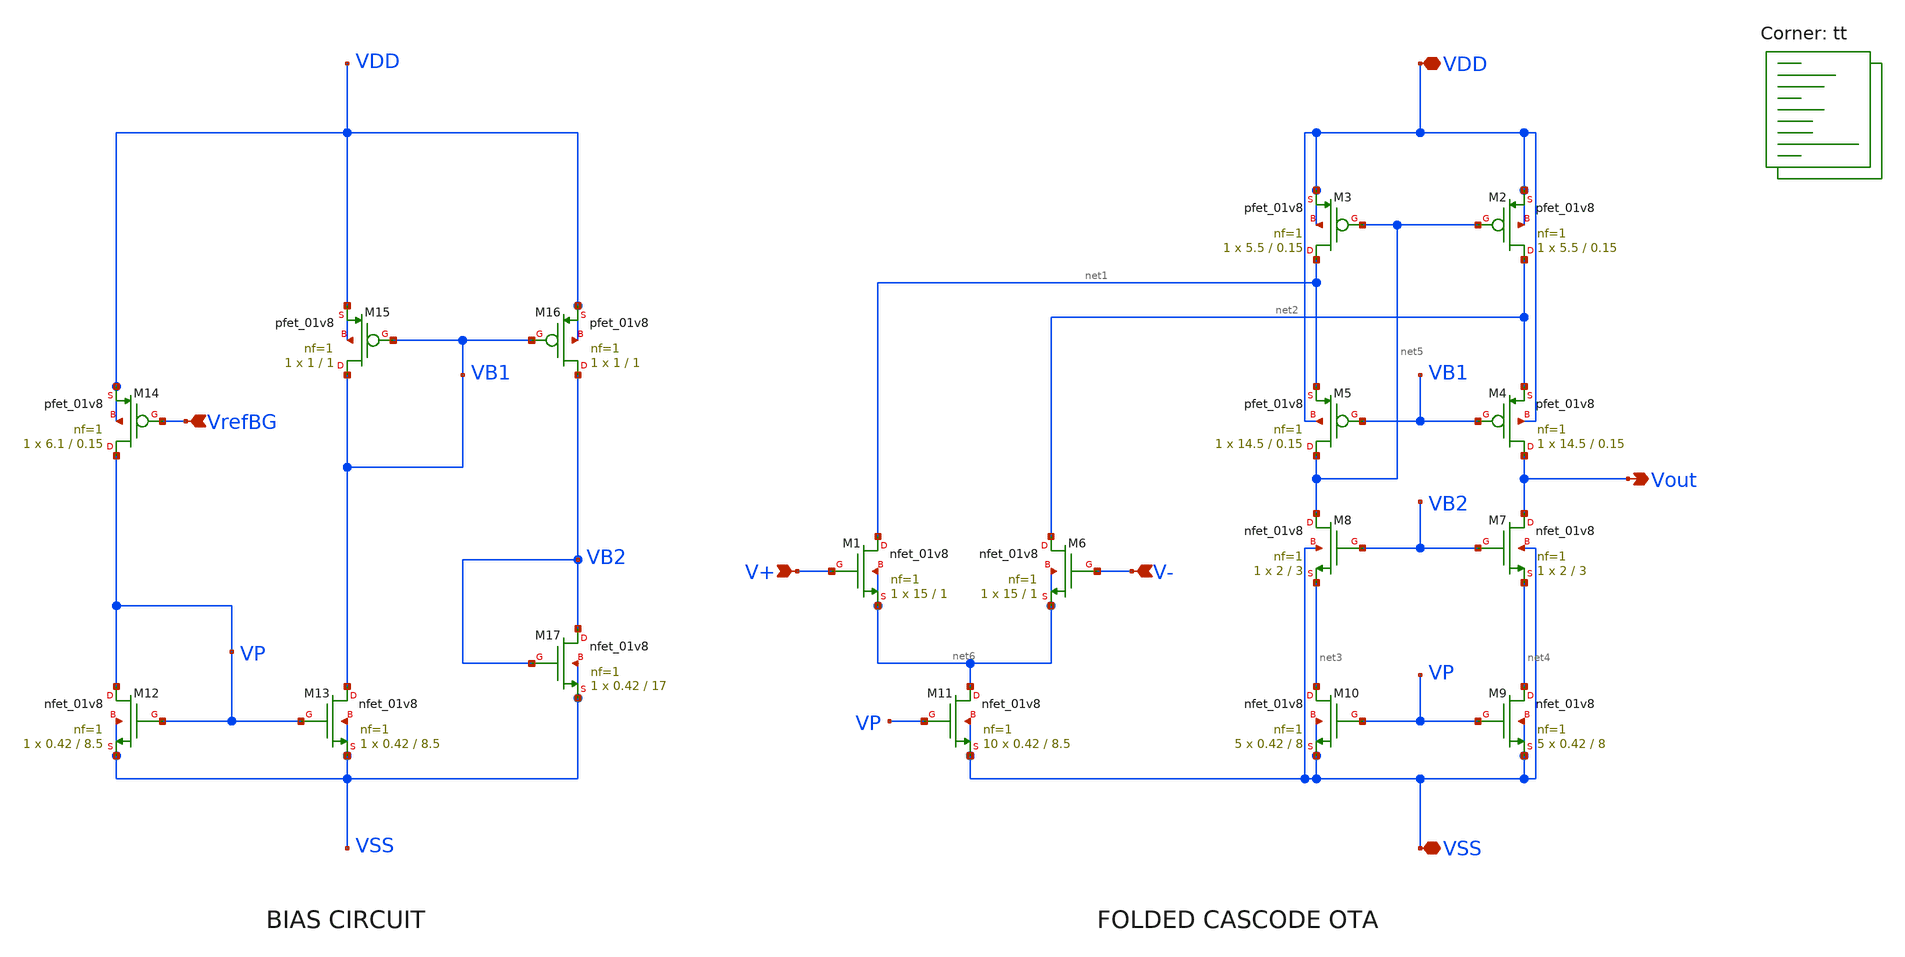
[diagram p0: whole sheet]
** sch_path: openfasoc/generators/curref-gen/sch/Folded_cascode_test.sch
**.subckt Folded_cascode_test Vout VSS V+ VDD V- VrefBG
*.opin Vout
*.iopin VSS
*.ipin V+
*.iopin VDD
*.ipin V-
*.ipin VrefBG
XM2 net2 net5 VDD VDD sky130_fd_pr__pfet_01v8 L=0.15 W=5.5 nf=1 ad='int((nf+1)/2) * W/nf * 0.29' as='int((nf+2)/2) * W/nf * 0.29'
+ pd='2*int((nf+1)/2) * (W/nf + 0.29)' ps='2*int((nf+2)/2) * (W/nf + 0.29)' nrd='0.29 / W' nrs='0.29 / W'
+ sa=0 sb=0 sd=0 mult=1 m=1
XM3 net1 net5 VDD VDD sky130_fd_pr__pfet_01v8 L=0.15 W=5.5 nf=1 ad='int((nf+1)/2) * W/nf * 0.29' as='int((nf+2)/2) * W/nf * 0.29'
+ pd='2*int((nf+1)/2) * (W/nf + 0.29)' ps='2*int((nf+2)/2) * (W/nf + 0.29)' nrd='0.29 / W' nrs='0.29 / W'
+ sa=0 sb=0 sd=0 mult=1 m=1
XM4 Vout VB1 net2 VDD sky130_fd_pr__pfet_01v8 L=0.15 W=14.5 nf=1 ad='int((nf+1)/2) * W/nf * 0.29' as='int((nf+2)/2) * W/nf * 0.29'
+ pd='2*int((nf+1)/2) * (W/nf + 0.29)' ps='2*int((nf+2)/2) * (W/nf + 0.29)' nrd='0.29 / W' nrs='0.29 / W'
+ sa=0 sb=0 sd=0 mult=1 m=1
XM5 net5 VB1 net1 VDD sky130_fd_pr__pfet_01v8 L=0.15 W=14.5 nf=1 ad='int((nf+1)/2) * W/nf * 0.29' as='int((nf+2)/2) * W/nf * 0.29'
+ pd='2*int((nf+1)/2) * (W/nf + 0.29)' ps='2*int((nf+2)/2) * (W/nf + 0.29)' nrd='0.29 / W' nrs='0.29 / W'
+ sa=0 sb=0 sd=0 mult=1 m=1
XM6 net2 V- net6 net6 sky130_fd_pr__nfet_01v8 L=1 W=15 nf=1 ad='int((nf+1)/2) * W/nf * 0.29' as='int((nf+2)/2) * W/nf * 0.29'
+ pd='2*int((nf+1)/2) * (W/nf + 0.29)' ps='2*int((nf+2)/2) * (W/nf + 0.29)' nrd='0.29 / W' nrs='0.29 / W'
+ sa=0 sb=0 sd=0 mult=1 m=1
XM7 Vout VB2 net4 VSS sky130_fd_pr__nfet_01v8 L=3 W=2 nf=1 ad='int((nf+1)/2) * W/nf * 0.29' as='int((nf+2)/2) * W/nf * 0.29'
+ pd='2*int((nf+1)/2) * (W/nf + 0.29)' ps='2*int((nf+2)/2) * (W/nf + 0.29)' nrd='0.29 / W' nrs='0.29 / W'
+ sa=0 sb=0 sd=0 mult=1 m=1
XM8 net5 VB2 net3 VSS sky130_fd_pr__nfet_01v8 L=3 W=2 nf=1 ad='int((nf+1)/2) * W/nf * 0.29' as='int((nf+2)/2) * W/nf * 0.29'
+ pd='2*int((nf+1)/2) * (W/nf + 0.29)' ps='2*int((nf+2)/2) * (W/nf + 0.29)' nrd='0.29 / W' nrs='0.29 / W'
+ sa=0 sb=0 sd=0 mult=1 m=1
XM9 net4 VP VSS VSS sky130_fd_pr__nfet_01v8 L=8 W=0.42 nf=1 ad='int((nf+1)/2) * W/nf * 0.29' as='int((nf+2)/2) * W/nf * 0.29'
+ pd='2*int((nf+1)/2) * (W/nf + 0.29)' ps='2*int((nf+2)/2) * (W/nf + 0.29)' nrd='0.29 / W' nrs='0.29 / W'
+ sa=0 sb=0 sd=0 mult=5 m=5
XM10 net3 VP VSS VSS sky130_fd_pr__nfet_01v8 L=8 W=0.42 nf=1 ad='int((nf+1)/2) * W/nf * 0.29' as='int((nf+2)/2) * W/nf * 0.29'
+ pd='2*int((nf+1)/2) * (W/nf + 0.29)' ps='2*int((nf+2)/2) * (W/nf + 0.29)' nrd='0.29 / W' nrs='0.29 / W'
+ sa=0 sb=0 sd=0 mult=5 m=5
XM11 net6 VP VSS VSS sky130_fd_pr__nfet_01v8 L=8.5 W=0.42 nf=1 ad='int((nf+1)/2) * W/nf * 0.29' as='int((nf+2)/2) * W/nf * 0.29'
+ pd='2*int((nf+1)/2) * (W/nf + 0.29)' ps='2*int((nf+2)/2) * (W/nf + 0.29)' nrd='0.29 / W' nrs='0.29 / W'
+ sa=0 sb=0 sd=0 mult=10 m=10
XM1 net1 V+ net6 net6 sky130_fd_pr__nfet_01v8 L=1 W=15 nf=1 ad='int((nf+1)/2) * W/nf * 0.29' as='int((nf+2)/2) * W/nf * 0.29'
+ pd='2*int((nf+1)/2) * (W/nf + 0.29)' ps='2*int((nf+2)/2) * (W/nf + 0.29)' nrd='0.29 / W' nrs='0.29 / W'
+ sa=0 sb=0 sd=0 mult=1 m=1
XM12 VP VP VSS VSS sky130_fd_pr__nfet_01v8 L=8.5 W=0.42 nf=1 ad='int((nf+1)/2) * W/nf * 0.29' as='int((nf+2)/2) * W/nf * 0.29'
+ pd='2*int((nf+1)/2) * (W/nf + 0.29)' ps='2*int((nf+2)/2) * (W/nf + 0.29)' nrd='0.29 / W' nrs='0.29 / W'
+ sa=0 sb=0 sd=0 mult=1 m=1
XM13 VB1 VP VSS VSS sky130_fd_pr__nfet_01v8 L=8.5 W=0.42 nf=1 ad='int((nf+1)/2) * W/nf * 0.29' as='int((nf+2)/2) * W/nf * 0.29'
+ pd='2*int((nf+1)/2) * (W/nf + 0.29)' ps='2*int((nf+2)/2) * (W/nf + 0.29)' nrd='0.29 / W' nrs='0.29 / W'
+ sa=0 sb=0 sd=0 mult=1 m=1
XM14 VP VrefBG VDD VDD sky130_fd_pr__pfet_01v8 L=0.15 W=6.1 nf=1 ad='int((nf+1)/2) * W/nf * 0.29' as='int((nf+2)/2) * W/nf * 0.29'
+ pd='2*int((nf+1)/2) * (W/nf + 0.29)' ps='2*int((nf+2)/2) * (W/nf + 0.29)' nrd='0.29 / W' nrs='0.29 / W'
+ sa=0 sb=0 sd=0 mult=1 m=1
XM15 VB1 VB1 VDD VDD sky130_fd_pr__pfet_01v8 L=1 W=1 nf=1 ad='int((nf+1)/2) * W/nf * 0.29' as='int((nf+2)/2) * W/nf * 0.29'
+ pd='2*int((nf+1)/2) * (W/nf + 0.29)' ps='2*int((nf+2)/2) * (W/nf + 0.29)' nrd='0.29 / W' nrs='0.29 / W'
+ sa=0 sb=0 sd=0 mult=1 m=1
XM16 VB2 VB1 VDD VDD sky130_fd_pr__pfet_01v8 L=1 W=1 nf=1 ad='int((nf+1)/2) * W/nf * 0.29' as='int((nf+2)/2) * W/nf * 0.29'
+ pd='2*int((nf+1)/2) * (W/nf + 0.29)' ps='2*int((nf+2)/2) * (W/nf + 0.29)' nrd='0.29 / W' nrs='0.29 / W'
+ sa=0 sb=0 sd=0 mult=1 m=1
XM17 VB2 VB2 VSS VSS sky130_fd_pr__nfet_01v8 L=17 W=0.42 nf=1 ad='int((nf+1)/2) * W/nf * 0.29' as='int((nf+2)/2) * W/nf * 0.29'
+ pd='2*int((nf+1)/2) * (W/nf + 0.29)' ps='2*int((nf+2)/2) * (W/nf + 0.29)' nrd='0.29 / W' nrs='0.29 / W'
+ sa=0 sb=0 sd=0 mult=1 m=1
**** begin user architecture code
.lib $::SKYWATER_MODELS/sky130.lib.spice tt
**** end user architecture code
**.ends
.end
